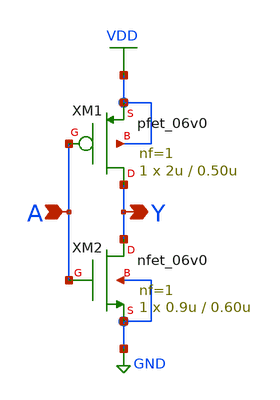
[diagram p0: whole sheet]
** sch_path: inv.sch
**.subckt inv Y A
*.opin Y
*.ipin A
XM1 Y A VDD VDD pfet_06v0 L=0.50u W=2u nf=1 ad='int((nf+1)/2) * W/nf * 0.18u' as='int((nf+2)/2) * W/nf * 0.18u'
+ pd='2*int((nf+1)/2) * (W/nf + 0.18u)' ps='2*int((nf+2)/2) * (W/nf + 0.18u)' nrd='0.18u / W' nrs='0.18u / W'
+ sa=0 sb=0 sd=0 m=1
XM2 Y A GND GND nfet_06v0 L=0.60u W=0.9u nf=1 ad='int((nf+1)/2) * W/nf * 0.18u' as='int((nf+2)/2) * W/nf * 0.18u'
+ pd='2*int((nf+1)/2) * (W/nf + 0.18u)' ps='2*int((nf+2)/2) * (W/nf + 0.18u)' nrd='0.18u / W' nrs='0.18u / W'
+ sa=0 sb=0 sd=0 m=1
**.ends
.GLOBAL GND
.GLOBAL VDD
.end
